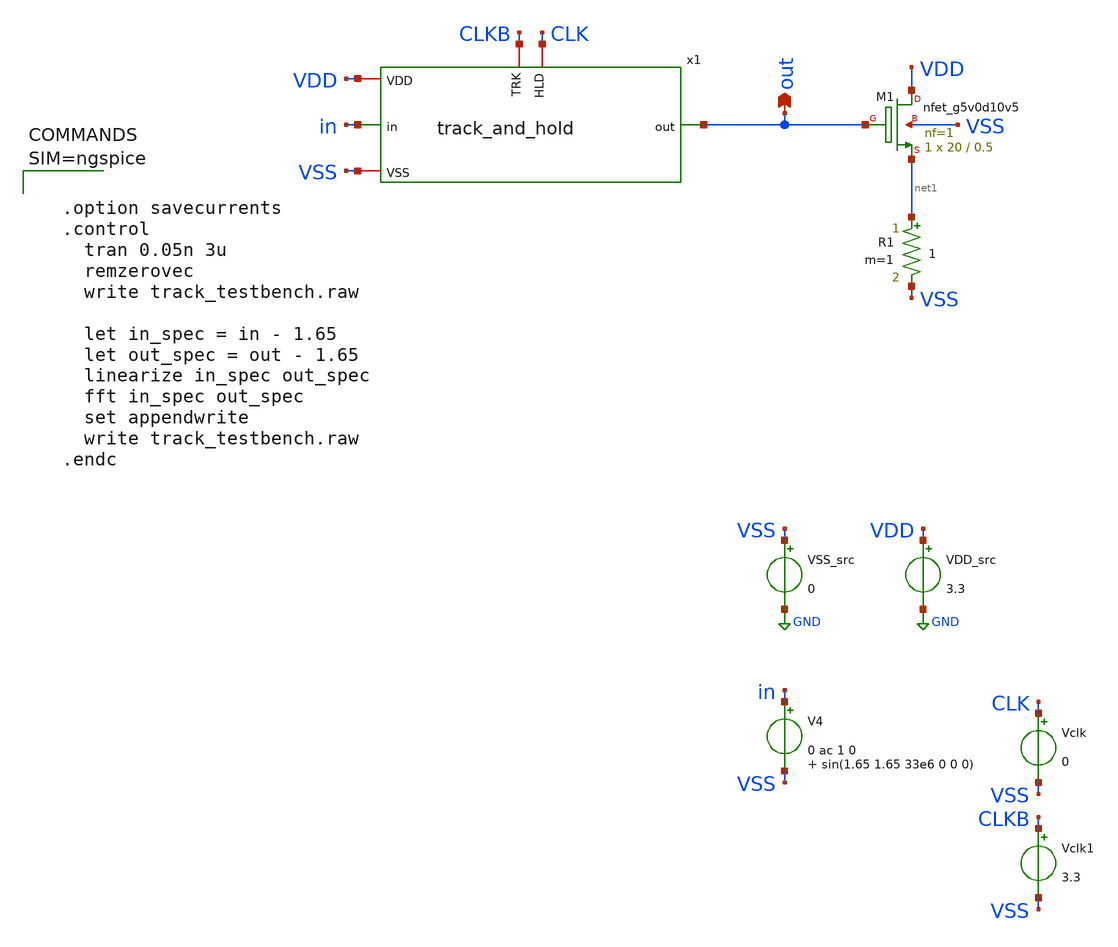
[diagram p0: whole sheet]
** sch_path: xschem/track_testbench.sch
**.subckt track_testbench out
*.opin out
VDD_src VDD GND 3.3
VSS_src VSS GND 0
V4 in VSS 0 ac 1 0 sin(1.65 1.65 33e6 0 0 0)
XM1 VDD out net1 VSS sky130_fd_pr__nfet_g5v0d10v5 L=0.5 W=20 nf=1 ad='int((nf+1)/2) * W/nf * 0.29' as='int((nf+2)/2) * W/nf * 0.29'
+ pd='2*int((nf+1)/2) * (W/nf + 0.29)' ps='2*int((nf+2)/2) * (W/nf + 0.29)' nrd='0.29 / W' nrs='0.29 / W'
+ sa=0 sb=0 sd=0 mult=1 m=1
R1 net1 VSS 1 m=1
Vclk CLK VSS 0
Vclk1 CLKB VSS 3.3
x1 CLK CLKB VDD VSS out in track_and_hold
**** begin user architecture code

** opencircuitdesign pdks install
.lib $::SKYWATER_MODELS/sky130.lib.spice tt





  .option savecurrents
  .control
    tran 0.05n 3u
    remzerovec
    write track_testbench.raw

    let in_spec = in - 1.65
    let out_spec = out - 1.65
    linearize in_spec out_spec
    fft in_spec out_spec
    set appendwrite
    write track_testbench.raw
  .endc



**** end user architecture code
**.ends

* expanding   symbol:  track_and_hold.sym # of pins=6
** sym_path: xschem/track_and_hold.sym
** sch_path: xschem/track_and_hold.sch
.subckt track_and_hold HLD TRK VDD VSS out in
*.iopin VSS
*.iopin VDD
*.ipin in
*.opin out
*.iopin TRK
*.iopin HLD
XC1 out VSS sky130_fd_pr__cap_mim_m3_1 W=5 L=5 MF=1 m=1
V1 net2 in 3.3
XM1 out net1 in VSS sky130_fd_pr__nfet_g5v0d10v5 L=0.5 W=1 nf=1 ad='int((nf+1)/2) * W/nf * 0.29' as='int((nf+2)/2) * W/nf * 0.29'
+ pd='2*int((nf+1)/2) * (W/nf + 0.29)' ps='2*int((nf+2)/2) * (W/nf + 0.29)' nrd='0.29 / W' nrs='0.29 / W'
+ sa=0 sb=0 sd=0 mult=1 m=1
R1 VDD VSS 1G m=1
S2 net1 net2 TRK VSS SWITCH1
S4 net1 VSS HLD VSS SWITCH1
**** begin user architecture code



.model switch1 sw vt=1.65 vh=0 ron=1 roff=1G



**** end user architecture code
V2 in net3 3.3
S2p net4 net3 TRK VSS SWITCH1
S4p net4 VDD HLD VSS SWITCH1
XM2 out net4 in VDD sky130_fd_pr__pfet_g5v0d10v5 L=0.5 W=1.28 nf=1 ad='int((nf+1)/2) * W/nf * 0.29' as='int((nf+2)/2) * W/nf * 0.29'
+ pd='2*int((nf+1)/2) * (W/nf + 0.29)' ps='2*int((nf+2)/2) * (W/nf + 0.29)' nrd='0.29 / W' nrs='0.29 / W'
+ sa=0 sb=0 sd=0 mult=1 m=1
.ends

.GLOBAL GND
.end
